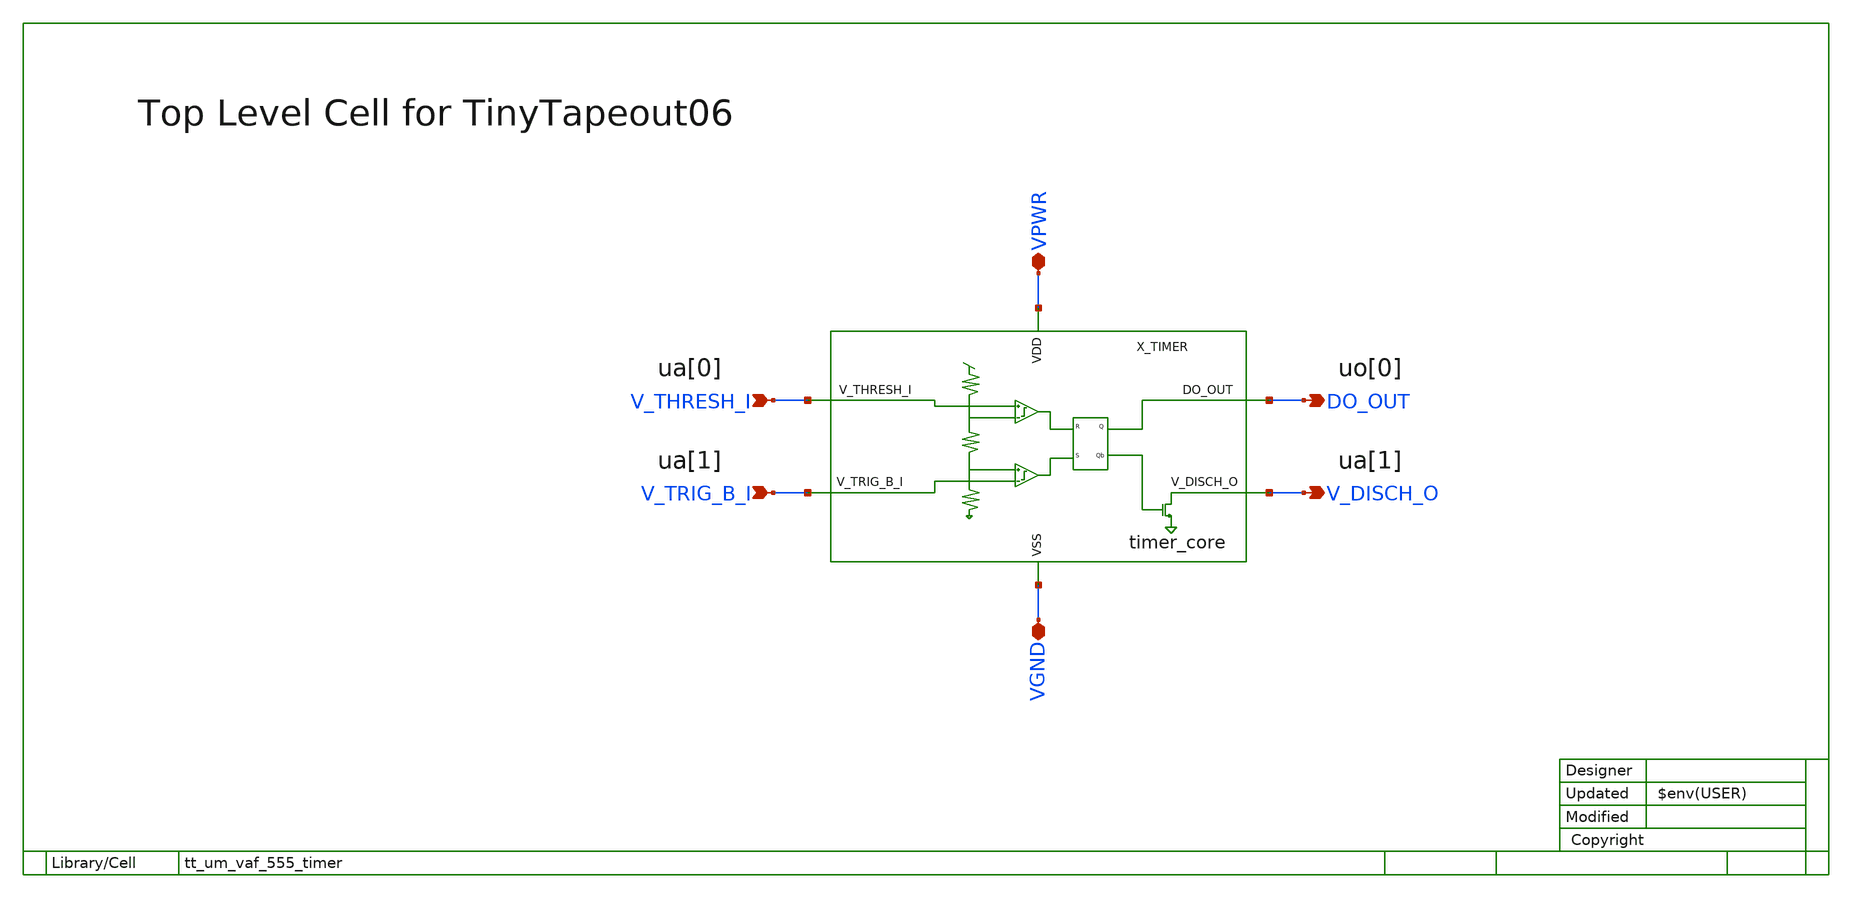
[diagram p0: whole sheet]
** sch_path: xsch/ip/top/tt_um_vaf_555_timer.sch
**.subckt tt_um_vaf_555_timer VPWR VGND DO_OUT V_THRESH_I V_TRIG_B_I V_DISCH_O
*.iopin VPWR
*.iopin VGND
*.opin DO_OUT
*.ipin V_THRESH_I
*.ipin V_TRIG_B_I
*.opin V_DISCH_O
X_TIMER VPWR DO_OUT VGND V_DISCH_O V_THRESH_I V_TRIG_B_I timer_core
**.ends
.end
